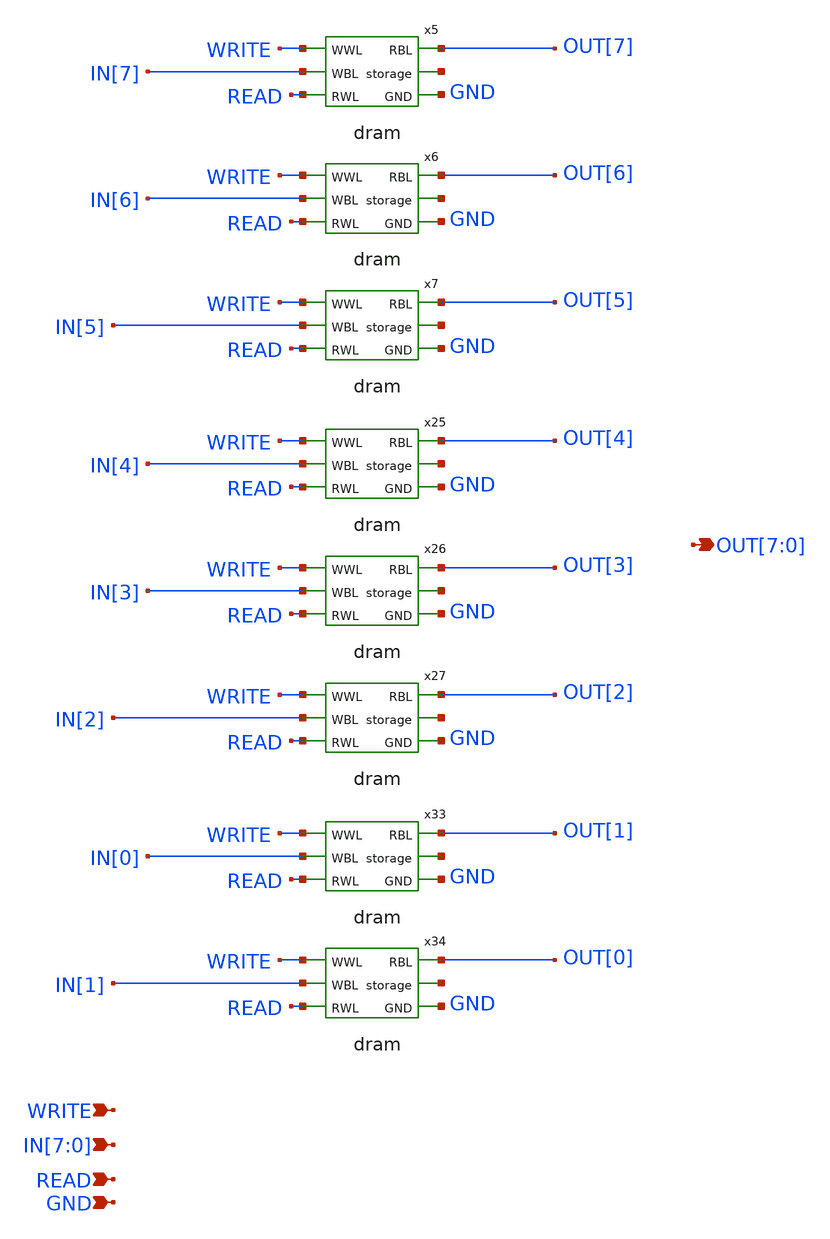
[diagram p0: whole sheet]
** sch_path: xschem/digital_prims/dram_8.sch
**.subckt dram_8 OUT[7],OUT[6],OUT[5],OUT[4],OUT[3],OUT[2],OUT[1],OUT[0] WRITE
*+ IN[7],IN[6],IN[5],IN[4],IN[3],IN[2],IN[1],IN[0] READ GND
*.opin OUT[7],OUT[6],OUT[5],OUT[4],OUT[3],OUT[2],OUT[1],OUT[0]
*.ipin WRITE
*.ipin IN[7],IN[6],IN[5],IN[4],IN[3],IN[2],IN[1],IN[0]
*.ipin READ
*.ipin GND
x5 WRITE OUT[7] net1 IN[7] READ GND dram
x6 WRITE OUT[6] net2 IN[6] READ GND dram
x7 WRITE OUT[5] net3 IN[5] READ GND dram
x25 WRITE OUT[4] net4 IN[4] READ GND dram
x26 WRITE OUT[3] net5 IN[3] READ GND dram
x27 WRITE OUT[2] net6 IN[2] READ GND dram
x33 WRITE OUT[1] net7 IN[0] READ GND dram
x34 WRITE OUT[0] net8 IN[1] READ GND dram
**.ends

* expanding   symbol:  digital_prims/dram.sym # of pins=6
** sym_path: xschem/digital_prims/dram.sym
** sch_path: xschem/digital_prims/dram.sch
.subckt dram WWL RBL storage WBL RWL GND
*.opin RBL
*.ipin RWL
*.ipin WBL
*.ipin WWL
*.opin storage
*.ipin GND
XM3 RWL storage RBL GND sky130_fd_pr__nfet_01v8 L=0.15 W=1 nf=1 ad='int((nf+1)/2) * W/nf * 0.29' as='int((nf+2)/2) * W/nf * 0.29'
+ pd='2*int((nf+1)/2) * (W/nf + 0.29)' ps='2*int((nf+2)/2) * (W/nf + 0.29)' nrd='0.29 / W' nrs='0.29 / W'
+ sa=0 sb=0 sd=0 mult=1 m=1
XM1 WBL WWL storage GND sky130_fd_pr__nfet_01v8 L=0.15 W=1 nf=1 ad='int((nf+1)/2) * W/nf * 0.29' as='int((nf+2)/2) * W/nf * 0.29'
+ pd='2*int((nf+1)/2) * (W/nf + 0.29)' ps='2*int((nf+2)/2) * (W/nf + 0.29)' nrd='0.29 / W' nrs='0.29 / W'
+ sa=0 sb=0 sd=0 mult=1 m=1
.ends

.end
